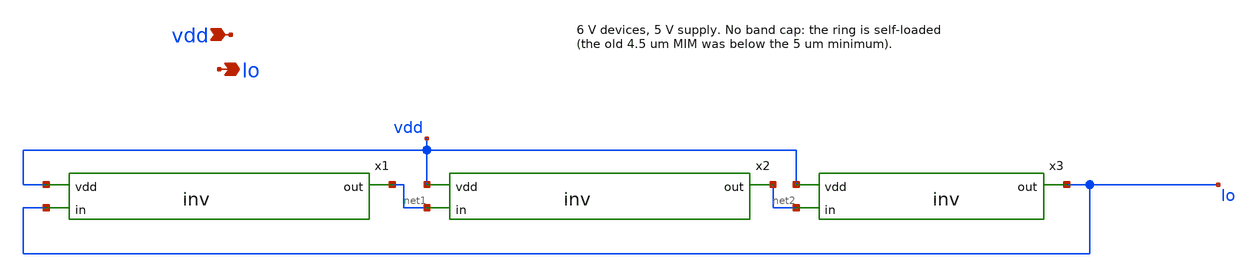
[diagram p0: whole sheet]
** sch_path: Schematics #2/xschem/ringosci.sch
**.subckt ringosci vdd lo
*.ipin vdd
*.opin lo
x1 net1 vdd lo inv
x2 net2 vdd net1 inv
x3 lo vdd net2 inv
**.ends

* expanding   symbol:  xschem/inv.sym # of pins=3
** sym_path: schematic pt2/xschem/inv.sym
** sch_path: schematic pt2/xschem/inv.sch
.subckt inv out vdd in
*.opin out
*.ipin vdd
*.ipin in
XM1 out in gnd GND nfet_03v3 L=0.28u W=wn nf=1 ad='int((nf+1)/2) * W/nf * 0.18u' as='int((nf+2)/2) * W/nf * 0.18u'
+ pd='2*int((nf+1)/2) * (W/nf + 0.18u)' ps='2*int((nf+2)/2) * (W/nf + 0.18u)' nrd='0.18u / W' nrs='0.18u / W'
+ sa=0 sb=0 sd=0 m=1 par=1
XM2 out in vdd VDD pfet_03v3 L=0.28u W=wp nf=1 ad='int((nf+1)/2) * W/nf * 0.18u' as='int((nf+2)/2) * W/nf * 0.18u'
+ pd='2*int((nf+1)/2) * (W/nf + 0.18u)' ps='2*int((nf+2)/2) * (W/nf + 0.18u)' nrd='0.18u / W' nrs='0.18u / W'
+ sa=0 sb=0 sd=0 m=1 par=1
.ends

.end
